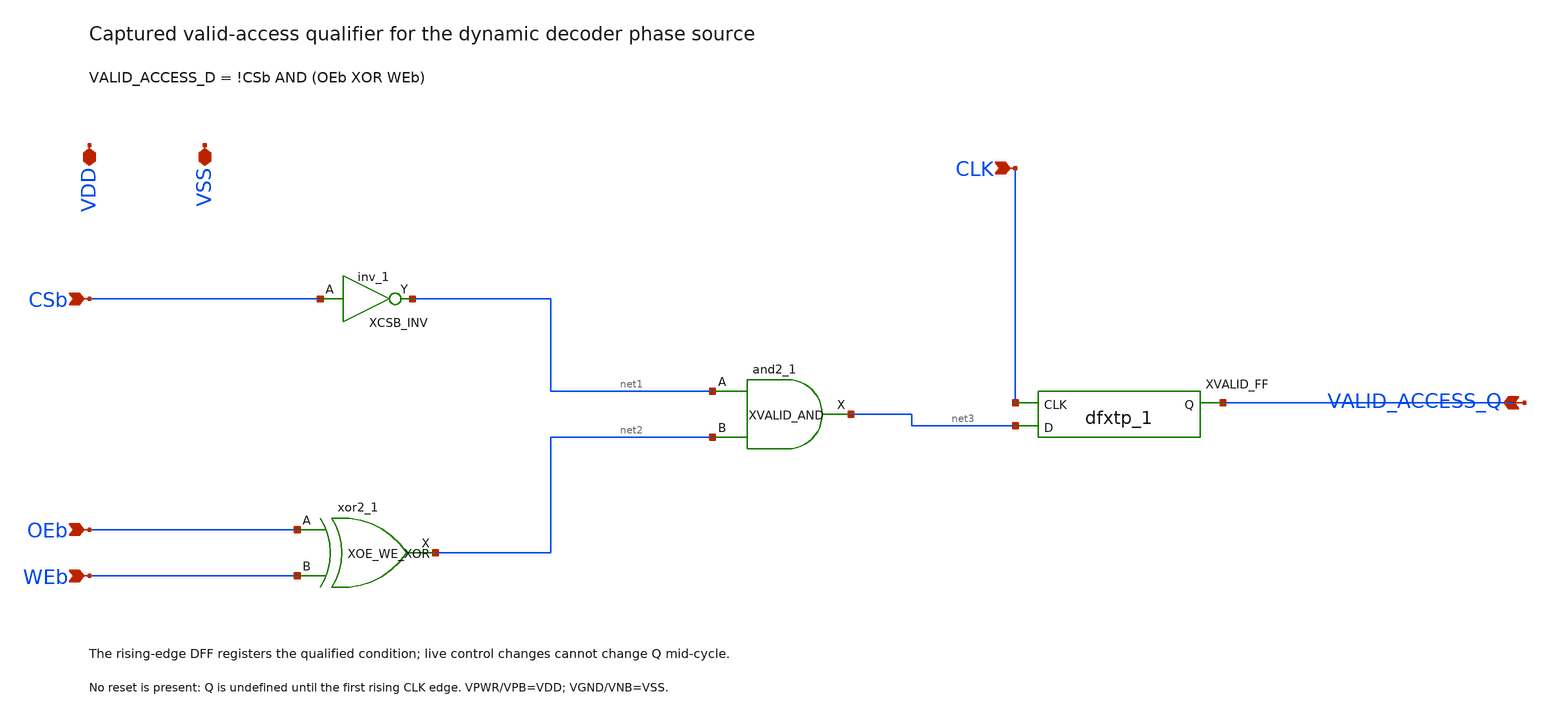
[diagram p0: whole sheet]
** sch_path: cells/control/valid_access_capture.sch
**.subckt valid_access_capture VDD VSS CSb OEb WEb CLK VALID_ACCESS_Q
*.iopin VDD
*.iopin VSS
*.ipin CSb
*.ipin OEb
*.ipin WEb
*.ipin CLK
*.opin VALID_ACCESS_Q
XCSB_INV CSb VSS VSS VDD VDD net1 sky130_fd_sc_hd__inv_1
XOE_WE_XOR OEb WEb VSS VSS VDD VDD net2 sky130_fd_sc_hd__xor2_1
XVALID_AND net1 net2 VSS VSS VDD VDD net3 sky130_fd_sc_hd__and2_1
XVALID_FF CLK net3 VSS VSS VDD VDD VALID_ACCESS_Q sky130_fd_sc_hd__dfxtp_1
**.ends
.end
